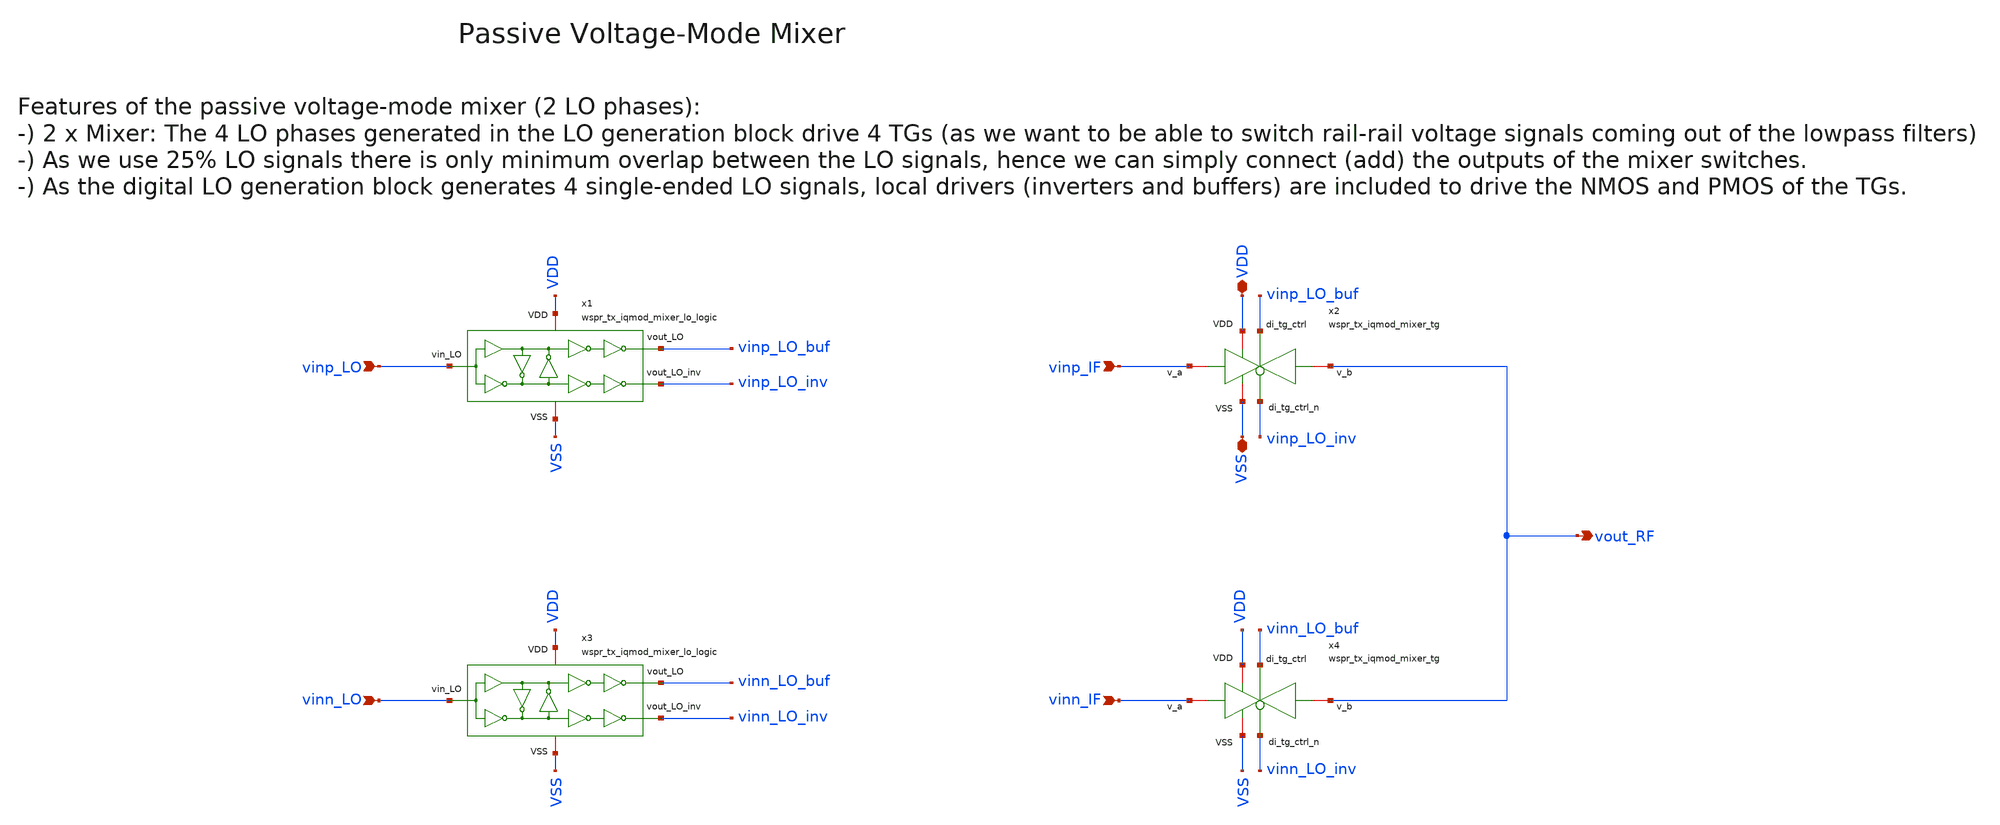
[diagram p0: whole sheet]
** sch_path: sky130/macros/iqmod/schematic/wspr_tx_iqmod_mixer.sch
**.subckt wspr_tx_iqmod_mixer VDD VSS vinp_IF vinn_IF vout_RF vinp_LO vinn_LO
*.iopin VDD
*.iopin VSS
*.ipin vinp_IF
*.ipin vinn_IF
*.opin vout_RF
*.ipin vinp_LO
*.ipin vinn_LO
x2 VDD vinp_LO_buf VSS vout_RF vinp_IF vinp_LO_inv wspr_tx_iqmod_mixer_tg
x4 VDD vinn_LO_buf VSS vout_RF vinn_IF vinn_LO_inv wspr_tx_iqmod_mixer_tg
x1 VDD vinp_LO vinp_LO_buf VSS vinp_LO_inv wspr_tx_iqmod_mixer_lo_logic
x3 VDD vinn_LO vinn_LO_buf VSS vinn_LO_inv wspr_tx_iqmod_mixer_lo_logic
**.ends
.end
